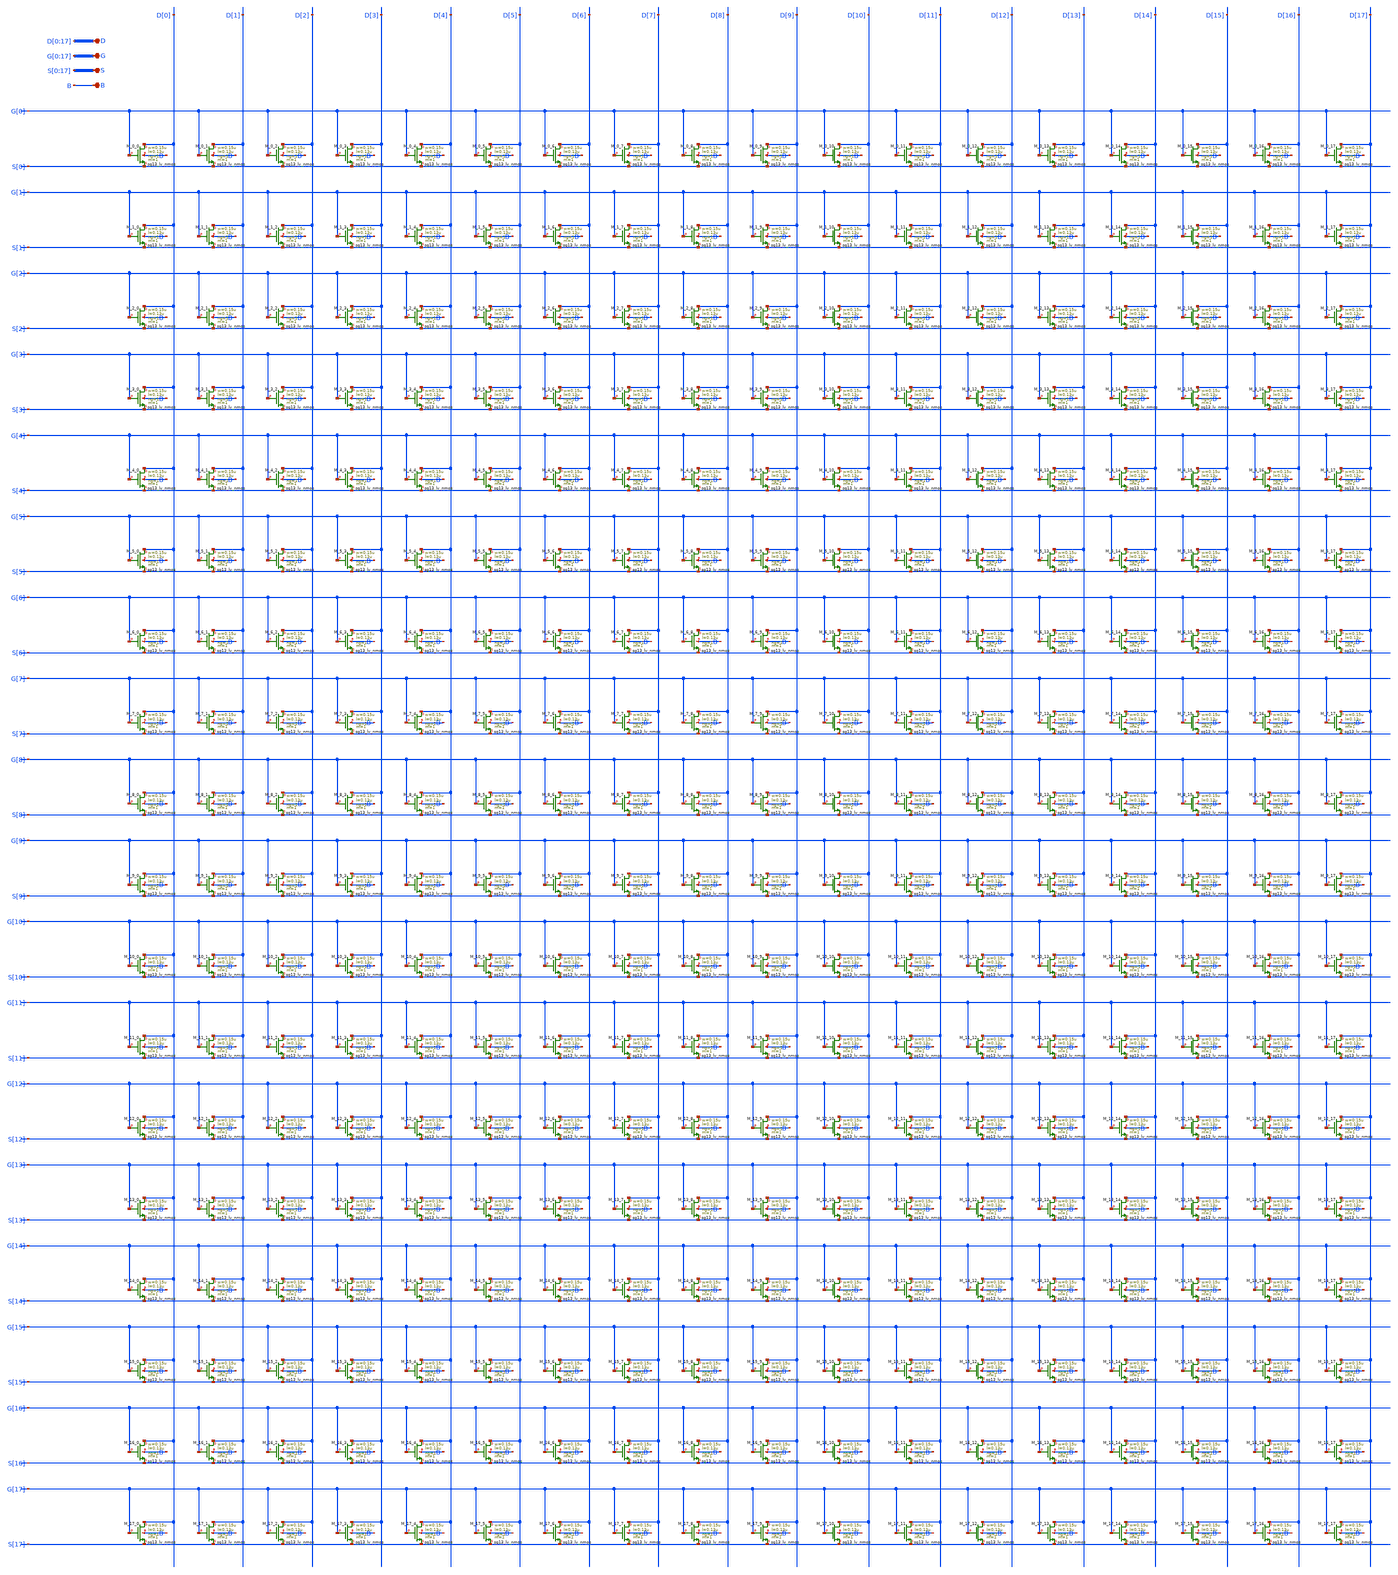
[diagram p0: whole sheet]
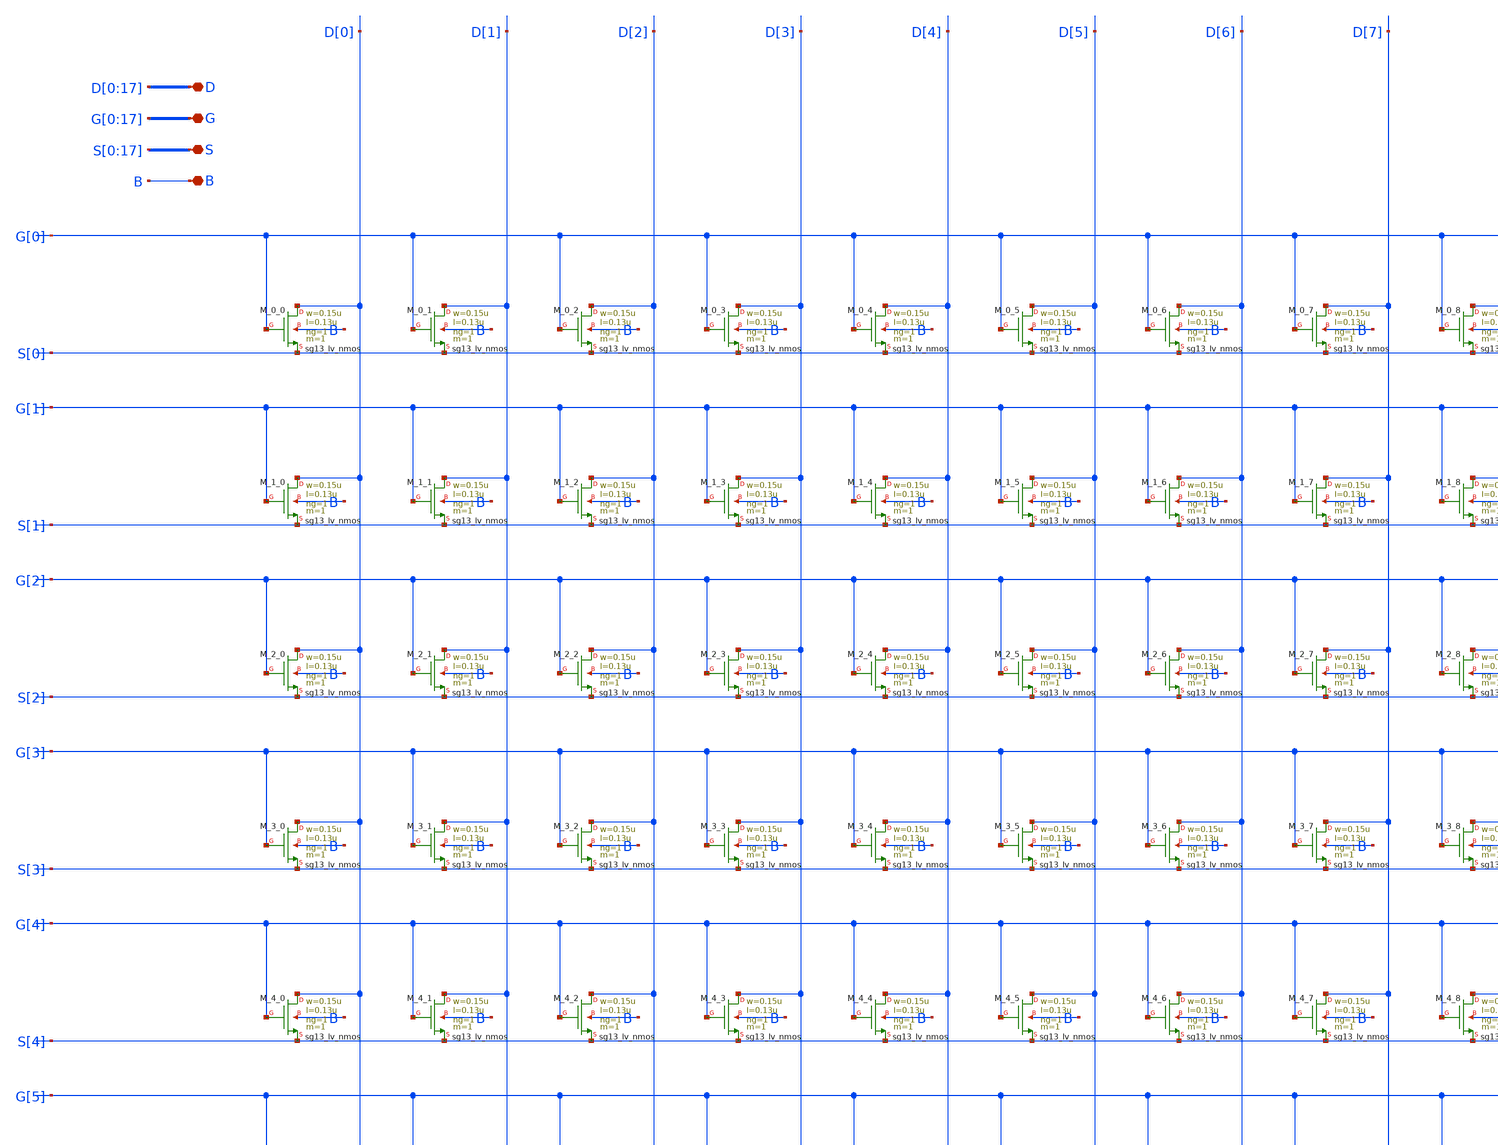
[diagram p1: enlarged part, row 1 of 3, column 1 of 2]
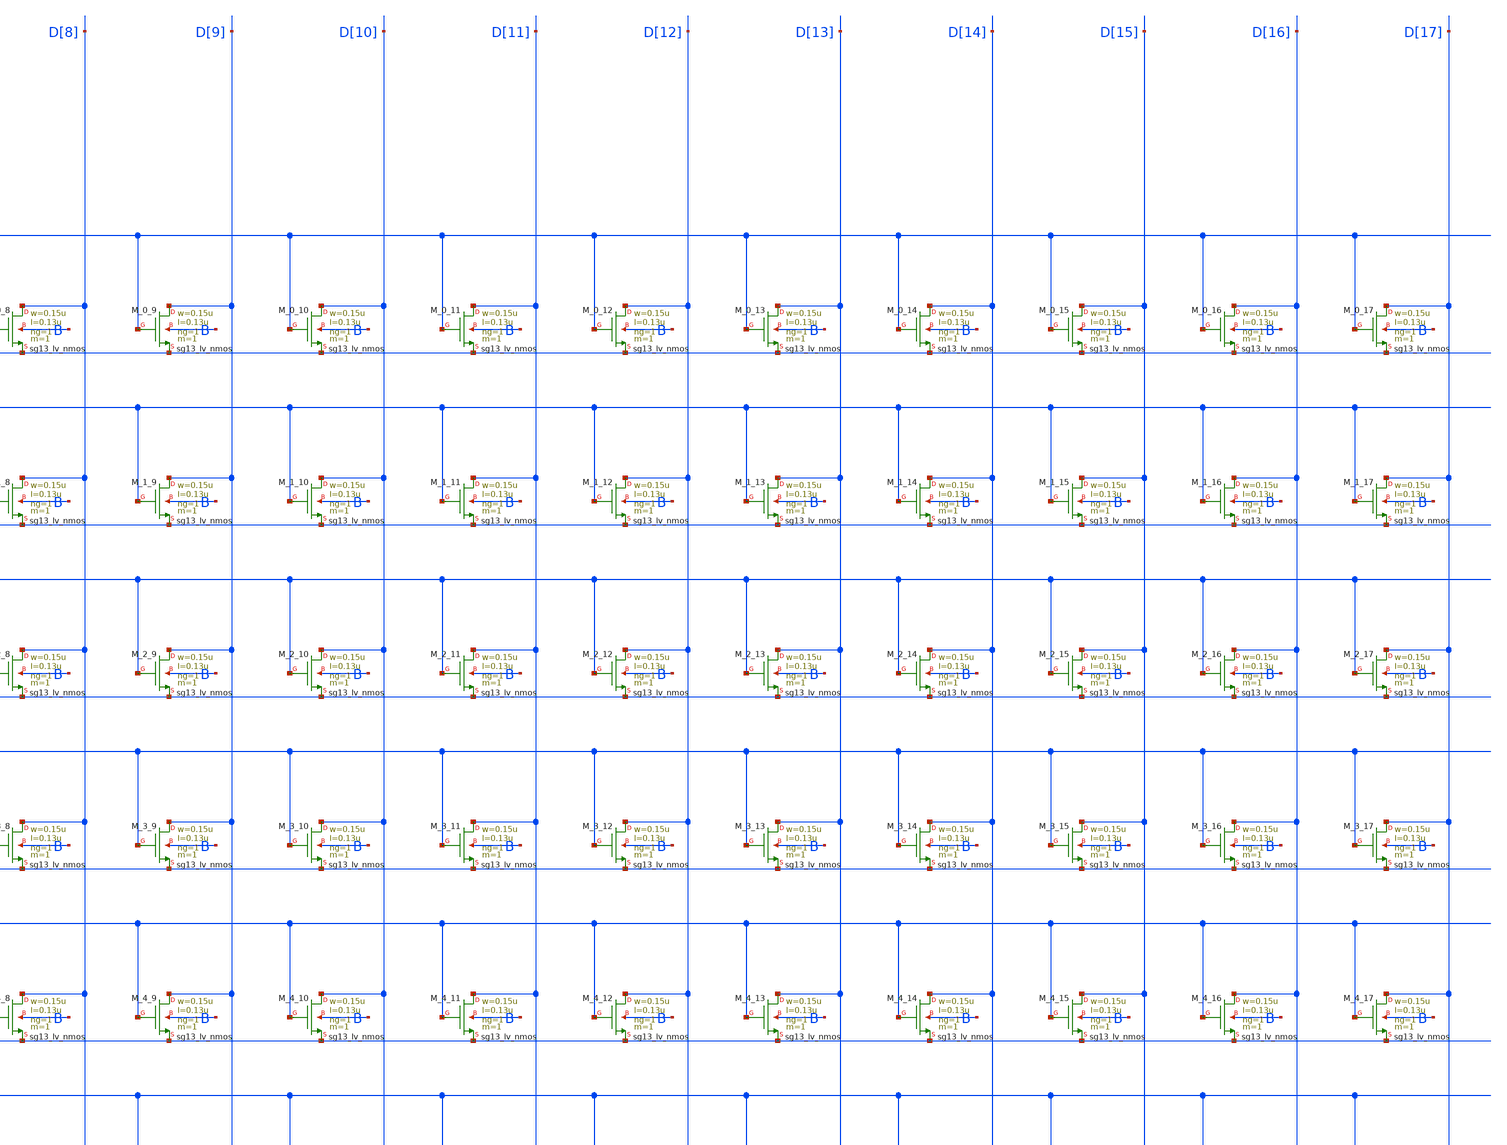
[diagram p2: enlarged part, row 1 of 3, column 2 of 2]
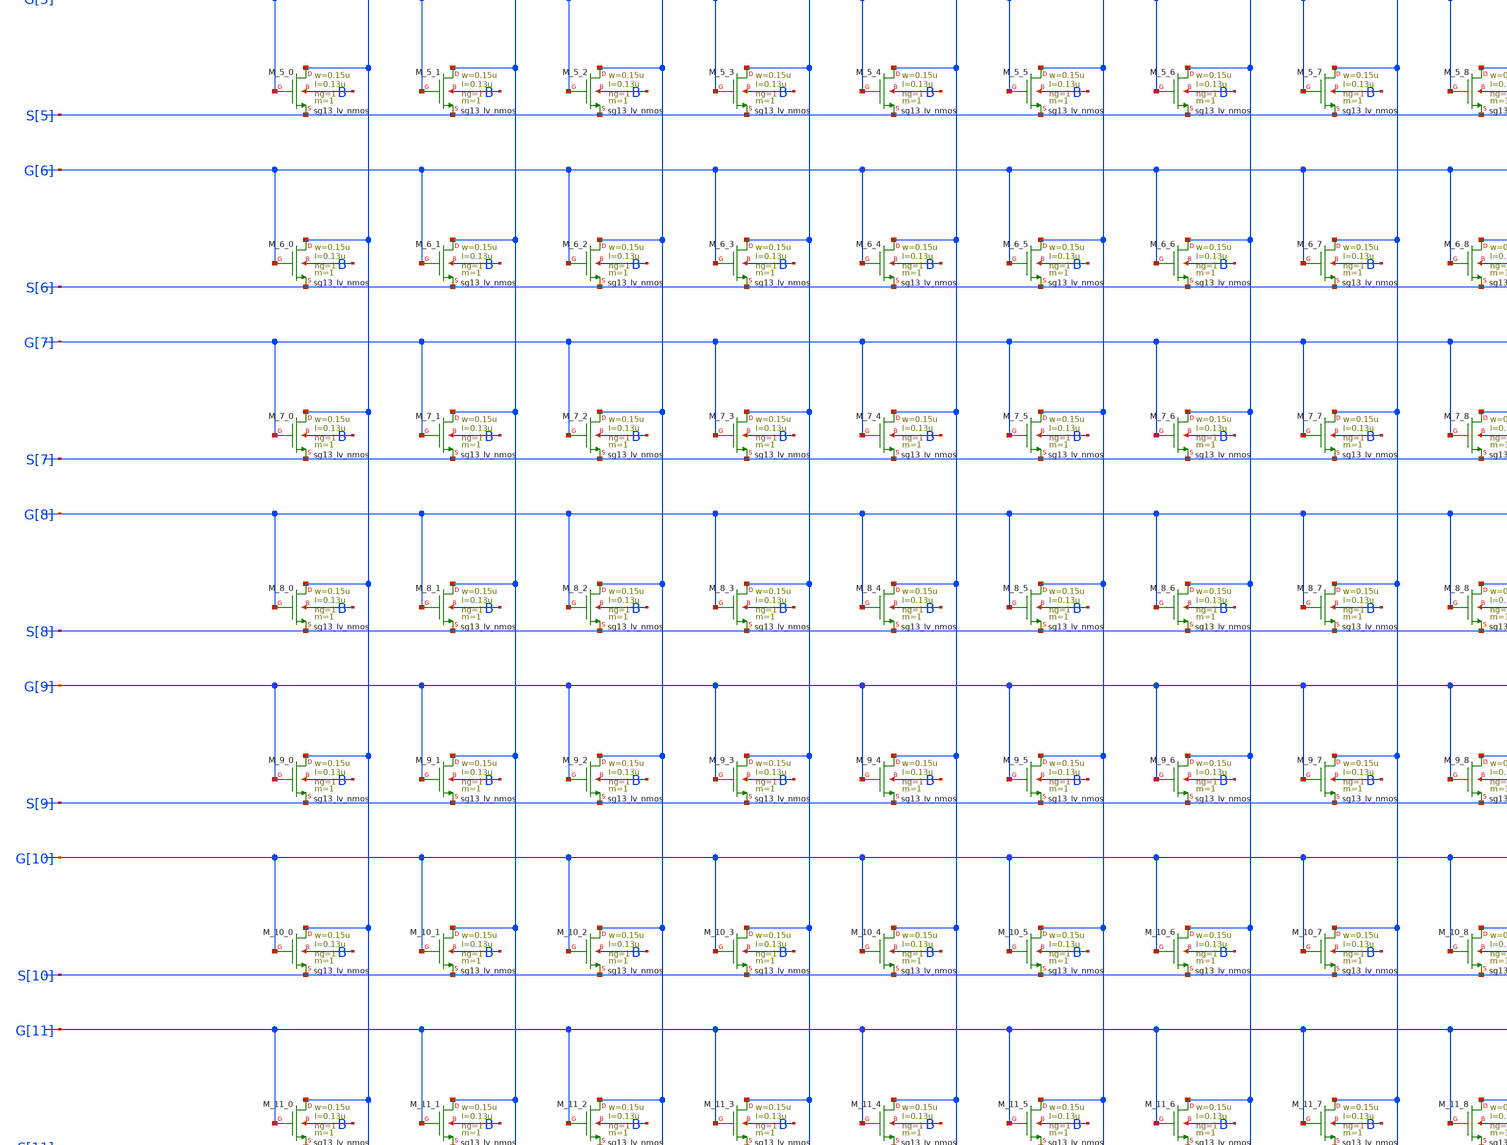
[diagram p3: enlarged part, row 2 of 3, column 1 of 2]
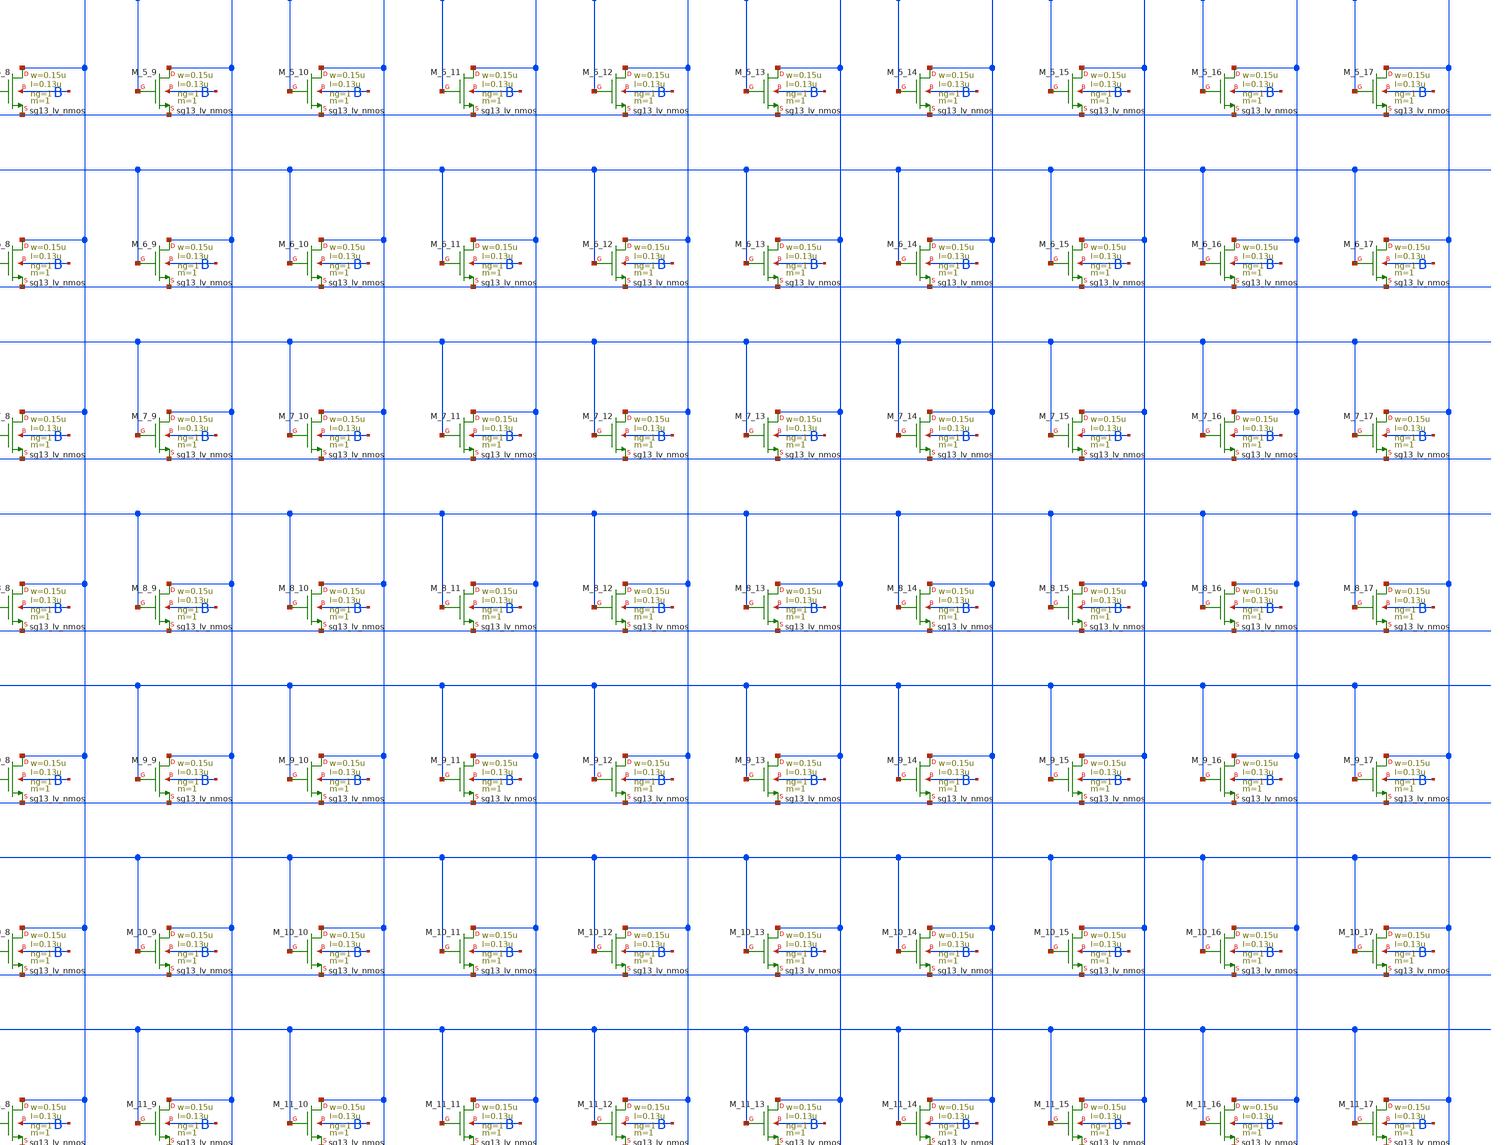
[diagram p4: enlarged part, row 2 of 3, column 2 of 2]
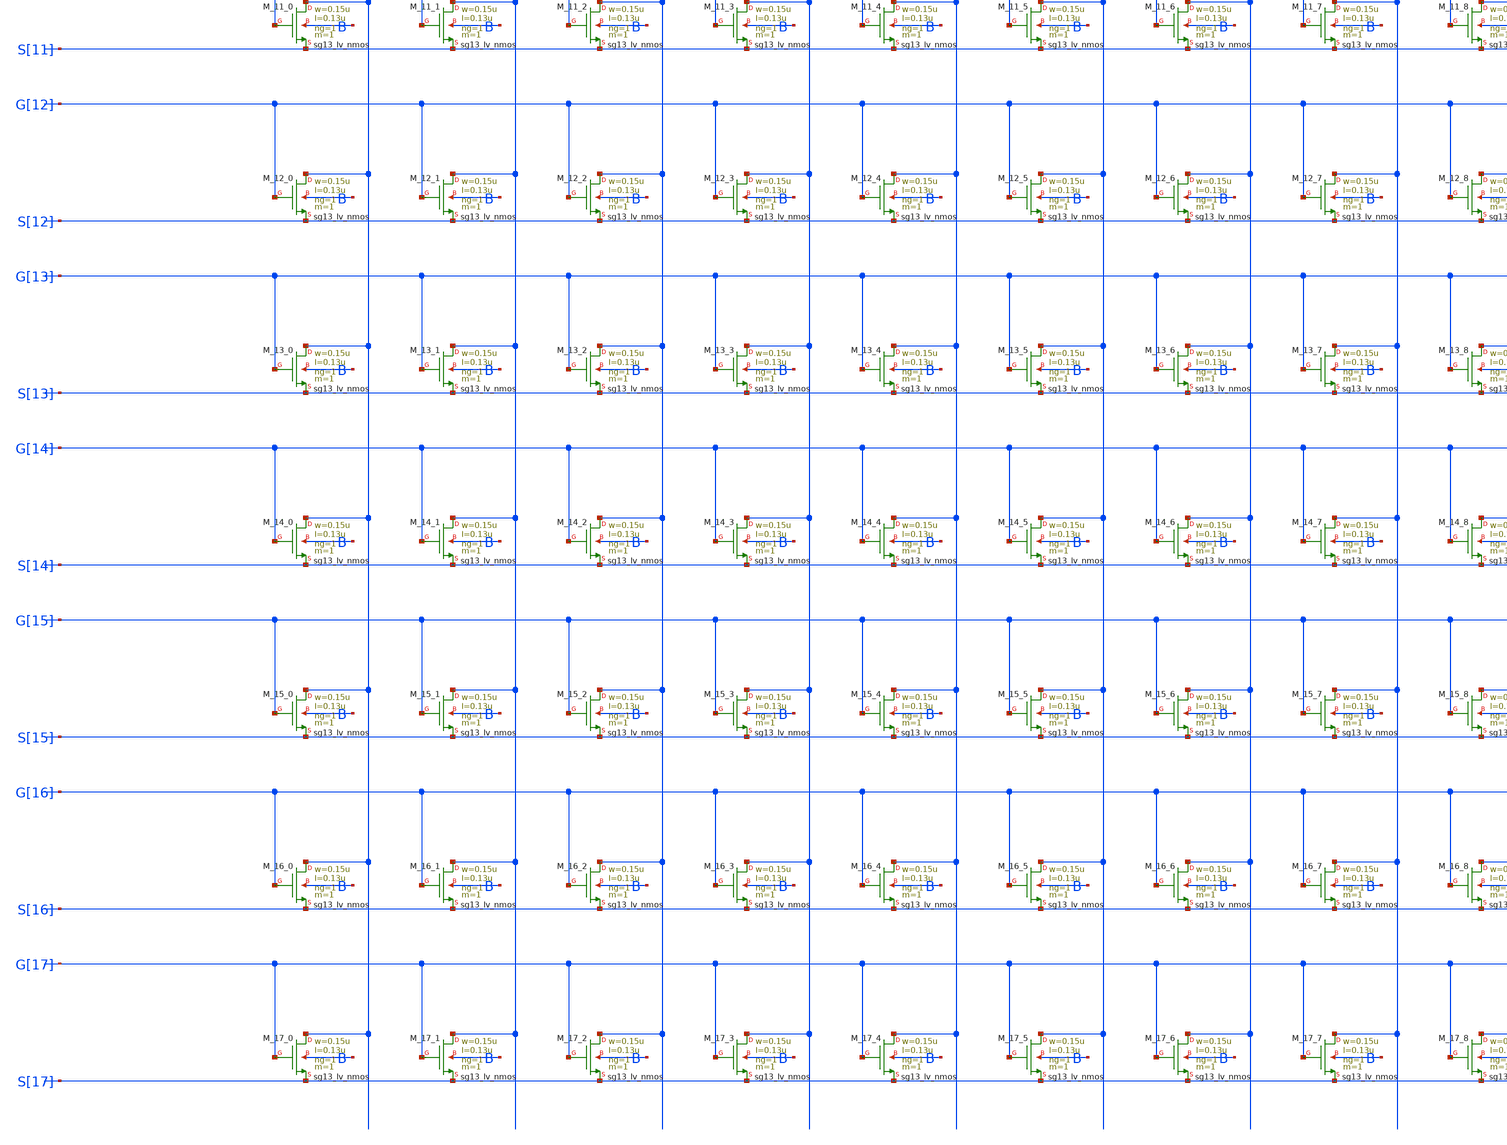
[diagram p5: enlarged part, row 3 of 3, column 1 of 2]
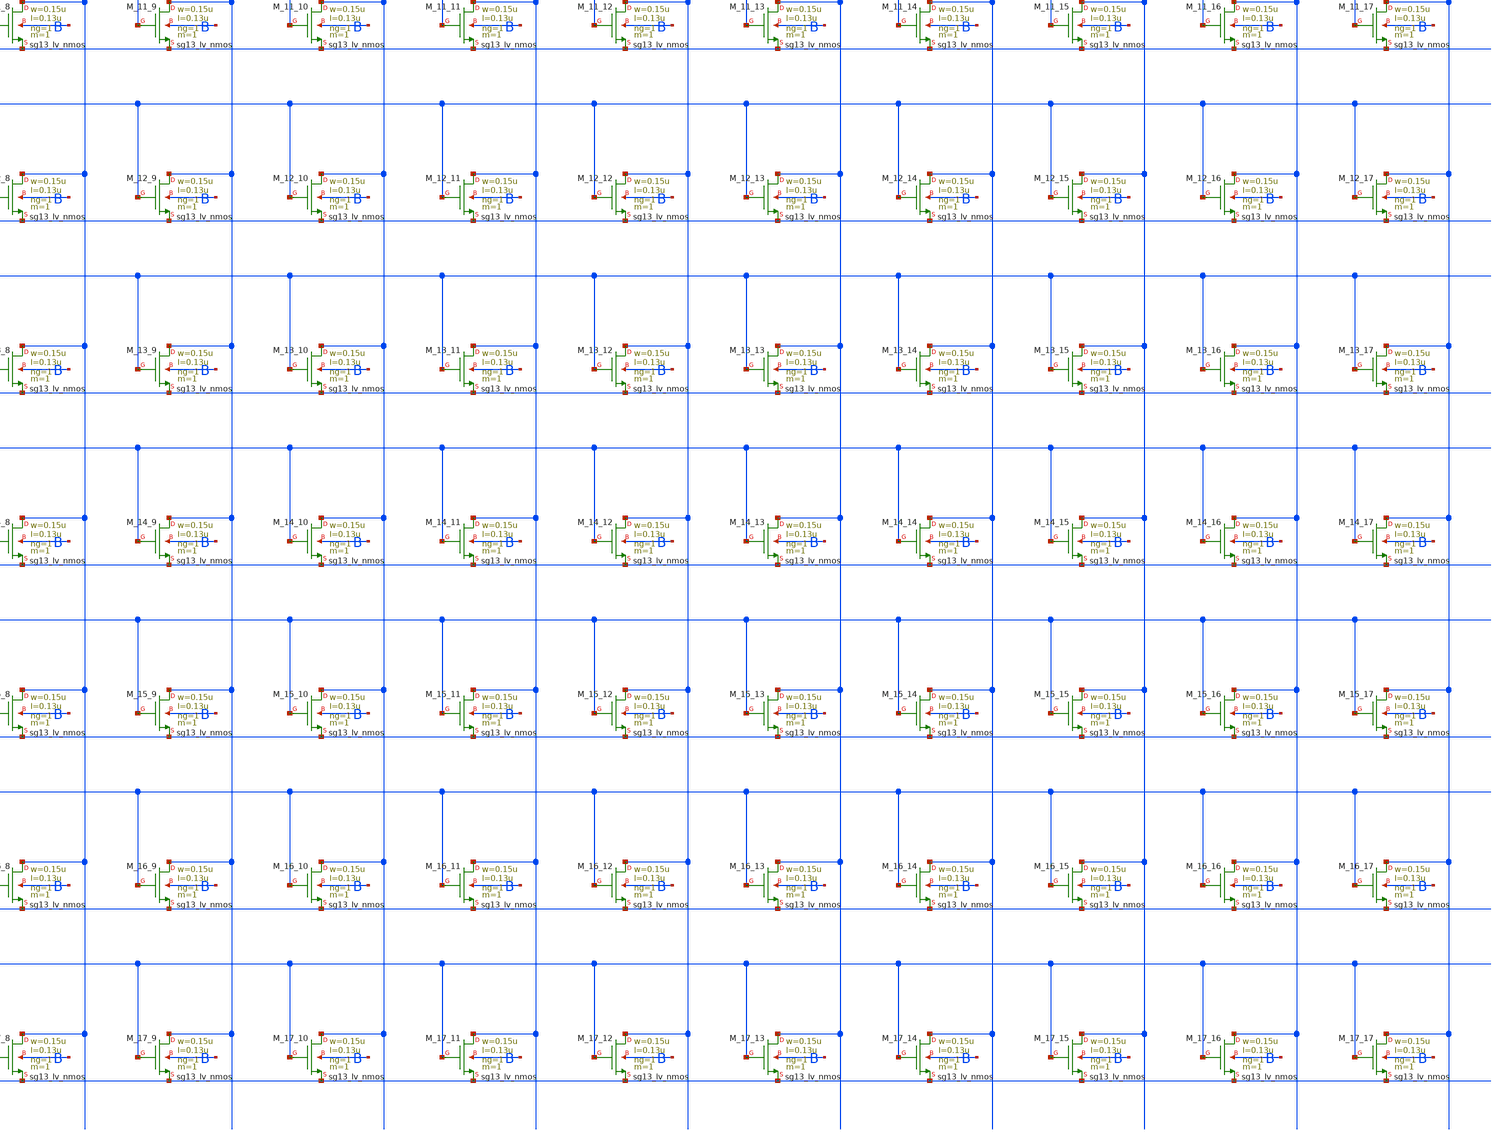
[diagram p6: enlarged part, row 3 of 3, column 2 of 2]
** sch_path: design_data/xschem/new_DUT/18x18/W0p15u_L0p13u.sch
**.subckt W0p15u_L0p13u D G S B
*.iopin D
*.iopin G
*.iopin S
*.iopin B
XM_0_0 D[0] G[0] S[0] B sg13_lv_nmos w=0.15u l=0.13u ng=1 m=1 mm_ok=1
XM_0_1 D[1] G[0] S[0] B sg13_lv_nmos w=0.15u l=0.13u ng=1 m=1 mm_ok=1
XM_0_2 D[2] G[0] S[0] B sg13_lv_nmos w=0.15u l=0.13u ng=1 m=1 mm_ok=1
XM_0_3 D[3] G[0] S[0] B sg13_lv_nmos w=0.15u l=0.13u ng=1 m=1 mm_ok=1
XM_0_4 D[4] G[0] S[0] B sg13_lv_nmos w=0.15u l=0.13u ng=1 m=1 mm_ok=1
XM_0_5 D[5] G[0] S[0] B sg13_lv_nmos w=0.15u l=0.13u ng=1 m=1 mm_ok=1
XM_0_6 D[6] G[0] S[0] B sg13_lv_nmos w=0.15u l=0.13u ng=1 m=1 mm_ok=1
XM_0_7 D[7] G[0] S[0] B sg13_lv_nmos w=0.15u l=0.13u ng=1 m=1 mm_ok=1
XM_0_8 D[8] G[0] S[0] B sg13_lv_nmos w=0.15u l=0.13u ng=1 m=1 mm_ok=1
XM_0_9 D[9] G[0] S[0] B sg13_lv_nmos w=0.15u l=0.13u ng=1 m=1 mm_ok=1
XM_0_10 D[10] G[0] S[0] B sg13_lv_nmos w=0.15u l=0.13u ng=1 m=1 mm_ok=1
XM_0_11 D[11] G[0] S[0] B sg13_lv_nmos w=0.15u l=0.13u ng=1 m=1 mm_ok=1
XM_0_12 D[12] G[0] S[0] B sg13_lv_nmos w=0.15u l=0.13u ng=1 m=1 mm_ok=1
XM_0_13 D[13] G[0] S[0] B sg13_lv_nmos w=0.15u l=0.13u ng=1 m=1 mm_ok=1
XM_0_14 D[14] G[0] S[0] B sg13_lv_nmos w=0.15u l=0.13u ng=1 m=1 mm_ok=1
XM_0_15 D[15] G[0] S[0] B sg13_lv_nmos w=0.15u l=0.13u ng=1 m=1 mm_ok=1
XM_0_16 D[16] G[0] S[0] B sg13_lv_nmos w=0.15u l=0.13u ng=1 m=1 mm_ok=1
XM_0_17 D[17] G[0] S[0] B sg13_lv_nmos w=0.15u l=0.13u ng=1 m=1 mm_ok=1
XM_1_0 D[0] G[1] S[1] B sg13_lv_nmos w=0.15u l=0.13u ng=1 m=1 mm_ok=1
XM_1_1 D[1] G[1] S[1] B sg13_lv_nmos w=0.15u l=0.13u ng=1 m=1 mm_ok=1
XM_1_2 D[2] G[1] S[1] B sg13_lv_nmos w=0.15u l=0.13u ng=1 m=1 mm_ok=1
XM_1_3 D[3] G[1] S[1] B sg13_lv_nmos w=0.15u l=0.13u ng=1 m=1 mm_ok=1
XM_1_4 D[4] G[1] S[1] B sg13_lv_nmos w=0.15u l=0.13u ng=1 m=1 mm_ok=1
XM_1_5 D[5] G[1] S[1] B sg13_lv_nmos w=0.15u l=0.13u ng=1 m=1 mm_ok=1
XM_1_6 D[6] G[1] S[1] B sg13_lv_nmos w=0.15u l=0.13u ng=1 m=1 mm_ok=1
XM_1_7 D[7] G[1] S[1] B sg13_lv_nmos w=0.15u l=0.13u ng=1 m=1 mm_ok=1
XM_1_8 D[8] G[1] S[1] B sg13_lv_nmos w=0.15u l=0.13u ng=1 m=1 mm_ok=1
XM_1_9 D[9] G[1] S[1] B sg13_lv_nmos w=0.15u l=0.13u ng=1 m=1 mm_ok=1
XM_1_10 D[10] G[1] S[1] B sg13_lv_nmos w=0.15u l=0.13u ng=1 m=1 mm_ok=1
XM_1_11 D[11] G[1] S[1] B sg13_lv_nmos w=0.15u l=0.13u ng=1 m=1 mm_ok=1
XM_1_12 D[12] G[1] S[1] B sg13_lv_nmos w=0.15u l=0.13u ng=1 m=1 mm_ok=1
XM_1_13 D[13] G[1] S[1] B sg13_lv_nmos w=0.15u l=0.13u ng=1 m=1 mm_ok=1
XM_1_14 D[14] G[1] S[1] B sg13_lv_nmos w=0.15u l=0.13u ng=1 m=1 mm_ok=1
XM_1_15 D[15] G[1] S[1] B sg13_lv_nmos w=0.15u l=0.13u ng=1 m=1 mm_ok=1
XM_1_16 D[16] G[1] S[1] B sg13_lv_nmos w=0.15u l=0.13u ng=1 m=1 mm_ok=1
XM_1_17 D[17] G[1] S[1] B sg13_lv_nmos w=0.15u l=0.13u ng=1 m=1 mm_ok=1
XM_2_0 D[0] G[2] S[2] B sg13_lv_nmos w=0.15u l=0.13u ng=1 m=1 mm_ok=1
XM_2_1 D[1] G[2] S[2] B sg13_lv_nmos w=0.15u l=0.13u ng=1 m=1 mm_ok=1
XM_2_2 D[2] G[2] S[2] B sg13_lv_nmos w=0.15u l=0.13u ng=1 m=1 mm_ok=1
XM_2_3 D[3] G[2] S[2] B sg13_lv_nmos w=0.15u l=0.13u ng=1 m=1 mm_ok=1
XM_2_4 D[4] G[2] S[2] B sg13_lv_nmos w=0.15u l=0.13u ng=1 m=1 mm_ok=1
XM_2_5 D[5] G[2] S[2] B sg13_lv_nmos w=0.15u l=0.13u ng=1 m=1 mm_ok=1
XM_2_6 D[6] G[2] S[2] B sg13_lv_nmos w=0.15u l=0.13u ng=1 m=1 mm_ok=1
XM_2_7 D[7] G[2] S[2] B sg13_lv_nmos w=0.15u l=0.13u ng=1 m=1 mm_ok=1
XM_2_8 D[8] G[2] S[2] B sg13_lv_nmos w=0.15u l=0.13u ng=1 m=1 mm_ok=1
XM_2_9 D[9] G[2] S[2] B sg13_lv_nmos w=0.15u l=0.13u ng=1 m=1 mm_ok=1
XM_2_10 D[10] G[2] S[2] B sg13_lv_nmos w=0.15u l=0.13u ng=1 m=1 mm_ok=1
XM_2_11 D[11] G[2] S[2] B sg13_lv_nmos w=0.15u l=0.13u ng=1 m=1 mm_ok=1
XM_2_12 D[12] G[2] S[2] B sg13_lv_nmos w=0.15u l=0.13u ng=1 m=1 mm_ok=1
XM_2_13 D[13] G[2] S[2] B sg13_lv_nmos w=0.15u l=0.13u ng=1 m=1 mm_ok=1
XM_2_14 D[14] G[2] S[2] B sg13_lv_nmos w=0.15u l=0.13u ng=1 m=1 mm_ok=1
XM_2_15 D[15] G[2] S[2] B sg13_lv_nmos w=0.15u l=0.13u ng=1 m=1 mm_ok=1
XM_2_16 D[16] G[2] S[2] B sg13_lv_nmos w=0.15u l=0.13u ng=1 m=1 mm_ok=1
XM_2_17 D[17] G[2] S[2] B sg13_lv_nmos w=0.15u l=0.13u ng=1 m=1 mm_ok=1
XM_3_0 D[0] G[3] S[3] B sg13_lv_nmos w=0.15u l=0.13u ng=1 m=1 mm_ok=1
XM_3_1 D[1] G[3] S[3] B sg13_lv_nmos w=0.15u l=0.13u ng=1 m=1 mm_ok=1
XM_3_2 D[2] G[3] S[3] B sg13_lv_nmos w=0.15u l=0.13u ng=1 m=1 mm_ok=1
XM_3_3 D[3] G[3] S[3] B sg13_lv_nmos w=0.15u l=0.13u ng=1 m=1 mm_ok=1
XM_3_4 D[4] G[3] S[3] B sg13_lv_nmos w=0.15u l=0.13u ng=1 m=1 mm_ok=1
XM_3_5 D[5] G[3] S[3] B sg13_lv_nmos w=0.15u l=0.13u ng=1 m=1 mm_ok=1
XM_3_6 D[6] G[3] S[3] B sg13_lv_nmos w=0.15u l=0.13u ng=1 m=1 mm_ok=1
XM_3_7 D[7] G[3] S[3] B sg13_lv_nmos w=0.15u l=0.13u ng=1 m=1 mm_ok=1
XM_3_8 D[8] G[3] S[3] B sg13_lv_nmos w=0.15u l=0.13u ng=1 m=1 mm_ok=1
XM_3_9 D[9] G[3] S[3] B sg13_lv_nmos w=0.15u l=0.13u ng=1 m=1 mm_ok=1
XM_3_10 D[10] G[3] S[3] B sg13_lv_nmos w=0.15u l=0.13u ng=1 m=1 mm_ok=1
XM_3_11 D[11] G[3] S[3] B sg13_lv_nmos w=0.15u l=0.13u ng=1 m=1 mm_ok=1
XM_3_12 D[12] G[3] S[3] B sg13_lv_nmos w=0.15u l=0.13u ng=1 m=1 mm_ok=1
XM_3_13 D[13] G[3] S[3] B sg13_lv_nmos w=0.15u l=0.13u ng=1 m=1 mm_ok=1
XM_3_14 D[14] G[3] S[3] B sg13_lv_nmos w=0.15u l=0.13u ng=1 m=1 mm_ok=1
XM_3_15 D[15] G[3] S[3] B sg13_lv_nmos w=0.15u l=0.13u ng=1 m=1 mm_ok=1
XM_3_16 D[16] G[3] S[3] B sg13_lv_nmos w=0.15u l=0.13u ng=1 m=1 mm_ok=1
XM_3_17 D[17] G[3] S[3] B sg13_lv_nmos w=0.15u l=0.13u ng=1 m=1 mm_ok=1
XM_4_0 D[0] G[4] S[4] B sg13_lv_nmos w=0.15u l=0.13u ng=1 m=1 mm_ok=1
XM_4_1 D[1] G[4] S[4] B sg13_lv_nmos w=0.15u l=0.13u ng=1 m=1 mm_ok=1
XM_4_2 D[2] G[4] S[4] B sg13_lv_nmos w=0.15u l=0.13u ng=1 m=1 mm_ok=1
XM_4_3 D[3] G[4] S[4] B sg13_lv_nmos w=0.15u l=0.13u ng=1 m=1 mm_ok=1
XM_4_4 D[4] G[4] S[4] B sg13_lv_nmos w=0.15u l=0.13u ng=1 m=1 mm_ok=1
XM_4_5 D[5] G[4] S[4] B sg13_lv_nmos w=0.15u l=0.13u ng=1 m=1 mm_ok=1
XM_4_6 D[6] G[4] S[4] B sg13_lv_nmos w=0.15u l=0.13u ng=1 m=1 mm_ok=1
XM_4_7 D[7] G[4] S[4] B sg13_lv_nmos w=0.15u l=0.13u ng=1 m=1 mm_ok=1
XM_4_8 D[8] G[4] S[4] B sg13_lv_nmos w=0.15u l=0.13u ng=1 m=1 mm_ok=1
XM_4_9 D[9] G[4] S[4] B sg13_lv_nmos w=0.15u l=0.13u ng=1 m=1 mm_ok=1
XM_4_10 D[10] G[4] S[4] B sg13_lv_nmos w=0.15u l=0.13u ng=1 m=1 mm_ok=1
XM_4_11 D[11] G[4] S[4] B sg13_lv_nmos w=0.15u l=0.13u ng=1 m=1 mm_ok=1
XM_4_12 D[12] G[4] S[4] B sg13_lv_nmos w=0.15u l=0.13u ng=1 m=1 mm_ok=1
XM_4_13 D[13] G[4] S[4] B sg13_lv_nmos w=0.15u l=0.13u ng=1 m=1 mm_ok=1
XM_4_14 D[14] G[4] S[4] B sg13_lv_nmos w=0.15u l=0.13u ng=1 m=1 mm_ok=1
XM_4_15 D[15] G[4] S[4] B sg13_lv_nmos w=0.15u l=0.13u ng=1 m=1 mm_ok=1
XM_4_16 D[16] G[4] S[4] B sg13_lv_nmos w=0.15u l=0.13u ng=1 m=1 mm_ok=1
XM_4_17 D[17] G[4] S[4] B sg13_lv_nmos w=0.15u l=0.13u ng=1 m=1 mm_ok=1
XM_5_0 D[0] G[5] S[5] B sg13_lv_nmos w=0.15u l=0.13u ng=1 m=1 mm_ok=1
XM_5_1 D[1] G[5] S[5] B sg13_lv_nmos w=0.15u l=0.13u ng=1 m=1 mm_ok=1
XM_5_2 D[2] G[5] S[5] B sg13_lv_nmos w=0.15u l=0.13u ng=1 m=1 mm_ok=1
XM_5_3 D[3] G[5] S[5] B sg13_lv_nmos w=0.15u l=0.13u ng=1 m=1 mm_ok=1
XM_5_4 D[4] G[5] S[5] B sg13_lv_nmos w=0.15u l=0.13u ng=1 m=1 mm_ok=1
XM_5_5 D[5] G[5] S[5] B sg13_lv_nmos w=0.15u l=0.13u ng=1 m=1 mm_ok=1
XM_5_6 D[6] G[5] S[5] B sg13_lv_nmos w=0.15u l=0.13u ng=1 m=1 mm_ok=1
XM_5_7 D[7] G[5] S[5] B sg13_lv_nmos w=0.15u l=0.13u ng=1 m=1 mm_ok=1
XM_5_8 D[8] G[5] S[5] B sg13_lv_nmos w=0.15u l=0.13u ng=1 m=1 mm_ok=1
XM_5_9 D[9] G[5] S[5] B sg13_lv_nmos w=0.15u l=0.13u ng=1 m=1 mm_ok=1
XM_5_10 D[10] G[5] S[5] B sg13_lv_nmos w=0.15u l=0.13u ng=1 m=1 mm_ok=1
XM_5_11 D[11] G[5] S[5] B sg13_lv_nmos w=0.15u l=0.13u ng=1 m=1 mm_ok=1
XM_5_12 D[12] G[5] S[5] B sg13_lv_nmos w=0.15u l=0.13u ng=1 m=1 mm_ok=1
XM_5_13 D[13] G[5] S[5] B sg13_lv_nmos w=0.15u l=0.13u ng=1 m=1 mm_ok=1
XM_5_14 D[14] G[5] S[5] B sg13_lv_nmos w=0.15u l=0.13u ng=1 m=1 mm_ok=1
XM_5_15 D[15] G[5] S[5] B sg13_lv_nmos w=0.15u l=0.13u ng=1 m=1 mm_ok=1
XM_5_16 D[16] G[5] S[5] B sg13_lv_nmos w=0.15u l=0.13u ng=1 m=1 mm_ok=1
XM_5_17 D[17] G[5] S[5] B sg13_lv_nmos w=0.15u l=0.13u ng=1 m=1 mm_ok=1
XM_6_0 D[0] G[6] S[6] B sg13_lv_nmos w=0.15u l=0.13u ng=1 m=1 mm_ok=1
XM_6_1 D[1] G[6] S[6] B sg13_lv_nmos w=0.15u l=0.13u ng=1 m=1 mm_ok=1
XM_6_2 D[2] G[6] S[6] B sg13_lv_nmos w=0.15u l=0.13u ng=1 m=1 mm_ok=1
XM_6_3 D[3] G[6] S[6] B sg13_lv_nmos w=0.15u l=0.13u ng=1 m=1 mm_ok=1
XM_6_4 D[4] G[6] S[6] B sg13_lv_nmos w=0.15u l=0.13u ng=1 m=1 mm_ok=1
XM_6_5 D[5] G[6] S[6] B sg13_lv_nmos w=0.15u l=0.13u ng=1 m=1 mm_ok=1
XM_6_6 D[6] G[6] S[6] B sg13_lv_nmos w=0.15u l=0.13u ng=1 m=1 mm_ok=1
XM_6_7 D[7] G[6] S[6] B sg13_lv_nmos w=0.15u l=0.13u ng=1 m=1 mm_ok=1
XM_6_8 D[8] G[6] S[6] B sg13_lv_nmos w=0.15u l=0.13u ng=1 m=1 mm_ok=1
XM_6_9 D[9] G[6] S[6] B sg13_lv_nmos w=0.15u l=0.13u ng=1 m=1 mm_ok=1
XM_6_10 D[10] G[6] S[6] B sg13_lv_nmos w=0.15u l=0.13u ng=1 m=1 mm_ok=1
XM_6_11 D[11] G[6] S[6] B sg13_lv_nmos w=0.15u l=0.13u ng=1 m=1 mm_ok=1
XM_6_12 D[12] G[6] S[6] B sg13_lv_nmos w=0.15u l=0.13u ng=1 m=1 mm_ok=1
XM_6_13 D[13] G[6] S[6] B sg13_lv_nmos w=0.15u l=0.13u ng=1 m=1 mm_ok=1
XM_6_14 D[14] G[6] S[6] B sg13_lv_nmos w=0.15u l=0.13u ng=1 m=1 mm_ok=1
XM_6_15 D[15] G[6] S[6] B sg13_lv_nmos w=0.15u l=0.13u ng=1 m=1 mm_ok=1
XM_6_16 D[16] G[6] S[6] B sg13_lv_nmos w=0.15u l=0.13u ng=1 m=1 mm_ok=1
XM_6_17 D[17] G[6] S[6] B sg13_lv_nmos w=0.15u l=0.13u ng=1 m=1 mm_ok=1
XM_7_0 D[0] G[7] S[7] B sg13_lv_nmos w=0.15u l=0.13u ng=1 m=1 mm_ok=1
XM_7_1 D[1] G[7] S[7] B sg13_lv_nmos w=0.15u l=0.13u ng=1 m=1 mm_ok=1
XM_7_2 D[2] G[7] S[7] B sg13_lv_nmos w=0.15u l=0.13u ng=1 m=1 mm_ok=1
XM_7_3 D[3] G[7] S[7] B sg13_lv_nmos w=0.15u l=0.13u ng=1 m=1 mm_ok=1
XM_7_4 D[4] G[7] S[7] B sg13_lv_nmos w=0.15u l=0.13u ng=1 m=1 mm_ok=1
XM_7_5 D[5] G[7] S[7] B sg13_lv_nmos w=0.15u l=0.13u ng=1 m=1 mm_ok=1
XM_7_6 D[6] G[7] S[7] B sg13_lv_nmos w=0.15u l=0.13u ng=1 m=1 mm_ok=1
XM_7_7 D[7] G[7] S[7] B sg13_lv_nmos w=0.15u l=0.13u ng=1 m=1 mm_ok=1
XM_7_8 D[8] G[7] S[7] B sg13_lv_nmos w=0.15u l=0.13u ng=1 m=1 mm_ok=1
XM_7_9 D[9] G[7] S[7] B sg13_lv_nmos w=0.15u l=0.13u ng=1 m=1 mm_ok=1
XM_7_10 D[10] G[7] S[7] B sg13_lv_nmos w=0.15u l=0.13u ng=1 m=1 mm_ok=1
XM_7_11 D[11] G[7] S[7] B sg13_lv_nmos w=0.15u l=0.13u ng=1 m=1 mm_ok=1
XM_7_12 D[12] G[7] S[7] B sg13_lv_nmos w=0.15u l=0.13u ng=1 m=1 mm_ok=1
XM_7_13 D[13] G[7] S[7] B sg13_lv_nmos w=0.15u l=0.13u ng=1 m=1 mm_ok=1
XM_7_14 D[14] G[7] S[7] B sg13_lv_nmos w=0.15u l=0.13u ng=1 m=1 mm_ok=1
XM_7_15 D[15] G[7] S[7] B sg13_lv_nmos w=0.15u l=0.13u ng=1 m=1 mm_ok=1
XM_7_16 D[16] G[7] S[7] B sg13_lv_nmos w=0.15u l=0.13u ng=1 m=1 mm_ok=1
XM_7_17 D[17] G[7] S[7] B sg13_lv_nmos w=0.15u l=0.13u ng=1 m=1 mm_ok=1
XM_8_0 D[0] G[8] S[8] B sg13_lv_nmos w=0.15u l=0.13u ng=1 m=1 mm_ok=1
XM_8_1 D[1] G[8] S[8] B sg13_lv_nmos w=0.15u l=0.13u ng=1 m=1 mm_ok=1
XM_8_2 D[2] G[8] S[8] B sg13_lv_nmos w=0.15u l=0.13u ng=1 m=1 mm_ok=1
XM_8_3 D[3] G[8] S[8] B sg13_lv_nmos w=0.15u l=0.13u ng=1 m=1 mm_ok=1
XM_8_4 D[4] G[8] S[8] B sg13_lv_nmos w=0.15u l=0.13u ng=1 m=1 mm_ok=1
XM_8_5 D[5] G[8] S[8] B sg13_lv_nmos w=0.15u l=0.13u ng=1 m=1 mm_ok=1
XM_8_6 D[6] G[8] S[8] B sg13_lv_nmos w=0.15u l=0.13u ng=1 m=1 mm_ok=1
XM_8_7 D[7] G[8] S[8] B sg13_lv_nmos w=0.15u l=0.13u ng=1 m=1 mm_ok=1
XM_8_8 D[8] G[8] S[8] B sg13_lv_nmos w=0.15u l=0.13u ng=1 m=1 mm_ok=1
XM_8_9 D[9] G[8] S[8] B sg13_lv_nmos w=0.15u l=0.13u ng=1 m=1 mm_ok=1
XM_8_10 D[10] G[8] S[8] B sg13_lv_nmos w=0.15u l=0.13u ng=1 m=1 mm_ok=1
XM_8_11 D[11] G[8] S[8] B sg13_lv_nmos w=0.15u l=0.13u ng=1 m=1 mm_ok=1
XM_8_12 D[12] G[8] S[8] B sg13_lv_nmos w=0.15u l=0.13u ng=1 m=1 mm_ok=1
XM_8_13 D[13] G[8] S[8] B sg13_lv_nmos w=0.15u l=0.13u ng=1 m=1 mm_ok=1
XM_8_14 D[14] G[8] S[8] B sg13_lv_nmos w=0.15u l=0.13u ng=1 m=1 mm_ok=1
XM_8_15 D[15] G[8] S[8] B sg13_lv_nmos w=0.15u l=0.13u ng=1 m=1 mm_ok=1
XM_8_16 D[16] G[8] S[8] B sg13_lv_nmos w=0.15u l=0.13u ng=1 m=1 mm_ok=1
XM_8_17 D[17] G[8] S[8] B sg13_lv_nmos w=0.15u l=0.13u ng=1 m=1 mm_ok=1
XM_9_0 D[0] G[9] S[9] B sg13_lv_nmos w=0.15u l=0.13u ng=1 m=1 mm_ok=1
XM_9_1 D[1] G[9] S[9] B sg13_lv_nmos w=0.15u l=0.13u ng=1 m=1 mm_ok=1
XM_9_2 D[2] G[9] S[9] B sg13_lv_nmos w=0.15u l=0.13u ng=1 m=1 mm_ok=1
XM_9_3 D[3] G[9] S[9] B sg13_lv_nmos w=0.15u l=0.13u ng=1 m=1 mm_ok=1
XM_9_4 D[4] G[9] S[9] B sg13_lv_nmos w=0.15u l=0.13u ng=1 m=1 mm_ok=1
XM_9_5 D[5] G[9] S[9] B sg13_lv_nmos w=0.15u l=0.13u ng=1 m=1 mm_ok=1
XM_9_6 D[6] G[9] S[9] B sg13_lv_nmos w=0.15u l=0.13u ng=1 m=1 mm_ok=1
XM_9_7 D[7] G[9] S[9] B sg13_lv_nmos w=0.15u l=0.13u ng=1 m=1 mm_ok=1
XM_9_8 D[8] G[9] S[9] B sg13_lv_nmos w=0.15u l=0.13u ng=1 m=1 mm_ok=1
XM_9_9 D[9] G[9] S[9] B sg13_lv_nmos w=0.15u l=0.13u ng=1 m=1 mm_ok=1
XM_9_10 D[10] G[9] S[9] B sg13_lv_nmos w=0.15u l=0.13u ng=1 m=1 mm_ok=1
XM_9_11 D[11] G[9] S[9] B sg13_lv_nmos w=0.15u l=0.13u ng=1 m=1 mm_ok=1
XM_9_12 D[12] G[9] S[9] B sg13_lv_nmos w=0.15u l=0.13u ng=1 m=1 mm_ok=1
XM_9_13 D[13] G[9] S[9] B sg13_lv_nmos w=0.15u l=0.13u ng=1 m=1 mm_ok=1
XM_9_14 D[14] G[9] S[9] B sg13_lv_nmos w=0.15u l=0.13u ng=1 m=1 mm_ok=1
XM_9_15 D[15] G[9] S[9] B sg13_lv_nmos w=0.15u l=0.13u ng=1 m=1 mm_ok=1
XM_9_16 D[16] G[9] S[9] B sg13_lv_nmos w=0.15u l=0.13u ng=1 m=1 mm_ok=1
XM_9_17 D[17] G[9] S[9] B sg13_lv_nmos w=0.15u l=0.13u ng=1 m=1 mm_ok=1
XM_10_0 D[0] G[10] S[10] B sg13_lv_nmos w=0.15u l=0.13u ng=1 m=1 mm_ok=1
XM_10_1 D[1] G[10] S[10] B sg13_lv_nmos w=0.15u l=0.13u ng=1 m=1 mm_ok=1
XM_10_2 D[2] G[10] S[10] B sg13_lv_nmos w=0.15u l=0.13u ng=1 m=1 mm_ok=1
XM_10_3 D[3] G[10] S[10] B sg13_lv_nmos w=0.15u l=0.13u ng=1 m=1 mm_ok=1
XM_10_4 D[4] G[10] S[10] B sg13_lv_nmos w=0.15u l=0.13u ng=1 m=1 mm_ok=1
XM_10_5 D[5] G[10] S[10] B sg13_lv_nmos w=0.15u l=0.13u ng=1 m=1 mm_ok=1
XM_10_6 D[6] G[10] S[10] B sg13_lv_nmos w=0.15u l=0.13u ng=1 m=1 mm_ok=1
XM_10_7 D[7] G[10] S[10] B sg13_lv_nmos w=0.15u l=0.13u ng=1 m=1 mm_ok=1
XM_10_8 D[8] G[10] S[10] B sg13_lv_nmos w=0.15u l=0.13u ng=1 m=1 mm_ok=1
XM_10_9 D[9] G[10] S[10] B sg13_lv_nmos w=0.15u l=0.13u ng=1 m=1 mm_ok=1
XM_10_10 D[10] G[10] S[10] B sg13_lv_nmos w=0.15u l=0.13u ng=1 m=1 mm_ok=1
XM_10_11 D[11] G[10] S[10] B sg13_lv_nmos w=0.15u l=0.13u ng=1 m=1 mm_ok=1
XM_10_12 D[12] G[10] S[10] B sg13_lv_nmos w=0.15u l=0.13u ng=1 m=1 mm_ok=1
XM_10_13 D[13] G[10] S[10] B sg13_lv_nmos w=0.15u l=0.13u ng=1 m=1 mm_ok=1
XM_10_14 D[14] G[10] S[10] B sg13_lv_nmos w=0.15u l=0.13u ng=1 m=1 mm_ok=1
XM_10_15 D[15] G[10] S[10] B sg13_lv_nmos w=0.15u l=0.13u ng=1 m=1 mm_ok=1
XM_10_16 D[16] G[10] S[10] B sg13_lv_nmos w=0.15u l=0.13u ng=1 m=1 mm_ok=1
XM_10_17 D[17] G[10] S[10] B sg13_lv_nmos w=0.15u l=0.13u ng=1 m=1 mm_ok=1
XM_11_0 D[0] G[11] S[11] B sg13_lv_nmos w=0.15u l=0.13u ng=1 m=1 mm_ok=1
XM_11_1 D[1] G[11] S[11] B sg13_lv_nmos w=0.15u l=0.13u ng=1 m=1 mm_ok=1
XM_11_2 D[2] G[11] S[11] B sg13_lv_nmos w=0.15u l=0.13u ng=1 m=1 mm_ok=1
XM_11_3 D[3] G[11] S[11] B sg13_lv_nmos w=0.15u l=0.13u ng=1 m=1 mm_ok=1
XM_11_4 D[4] G[11] S[11] B sg13_lv_nmos w=0.15u l=0.13u ng=1 m=1 mm_ok=1
XM_11_5 D[5] G[11] S[11] B sg13_lv_nmos w=0.15u l=0.13u ng=1 m=1 mm_ok=1
XM_11_6 D[6] G[11] S[11] B sg13_lv_nmos w=0.15u l=0.13u ng=1 m=1 mm_ok=1
XM_11_7 D[7] G[11] S[11] B sg13_lv_nmos w=0.15u l=0.13u ng=1 m=1 mm_ok=1
XM_11_8 D[8] G[11] S[11] B sg13_lv_nmos w=0.15u l=0.13u ng=1 m=1 mm_ok=1
XM_11_9 D[9] G[11] S[11] B sg13_lv_nmos w=0.15u l=0.13u ng=1 m=1 mm_ok=1
XM_11_10 D[10] G[11] S[11] B sg13_lv_nmos w=0.15u l=0.13u ng=1 m=1 mm_ok=1
XM_11_11 D[11] G[11] S[11] B sg13_lv_nmos w=0.15u l=0.13u ng=1 m=1 mm_ok=1
XM_11_12 D[12] G[11] S[11] B sg13_lv_nmos w=0.15u l=0.13u ng=1 m=1 mm_ok=1
XM_11_13 D[13] G[11] S[11] B sg13_lv_nmos w=0.15u l=0.13u ng=1 m=1 mm_ok=1
XM_11_14 D[14] G[11] S[11] B sg13_lv_nmos w=0.15u l=0.13u ng=1 m=1 mm_ok=1
XM_11_15 D[15] G[11] S[11] B sg13_lv_nmos w=0.15u l=0.13u ng=1 m=1 mm_ok=1
XM_11_16 D[16] G[11] S[11] B sg13_lv_nmos w=0.15u l=0.13u ng=1 m=1 mm_ok=1
XM_11_17 D[17] G[11] S[11] B sg13_lv_nmos w=0.15u l=0.13u ng=1 m=1 mm_ok=1
XM_12_0 D[0] G[12] S[12] B sg13_lv_nmos w=0.15u l=0.13u ng=1 m=1 mm_ok=1
XM_12_1 D[1] G[12] S[12] B sg13_lv_nmos w=0.15u l=0.13u ng=1 m=1 mm_ok=1
XM_12_2 D[2] G[12] S[12] B sg13_lv_nmos w=0.15u l=0.13u ng=1 m=1 mm_ok=1
XM_12_3 D[3] G[12] S[12] B sg13_lv_nmos w=0.15u l=0.13u ng=1 m=1 mm_ok=1
XM_12_4 D[4] G[12] S[12] B sg13_lv_nmos w=0.15u l=0.13u ng=1 m=1 mm_ok=1
XM_12_5 D[5] G[12] S[12] B sg13_lv_nmos w=0.15u l=0.13u ng=1 m=1 mm_ok=1
XM_12_6 D[6] G[12] S[12] B sg13_lv_nmos w=0.15u l=0.13u ng=1 m=1 mm_ok=1
XM_12_7 D[7] G[12] S[12] B sg13_lv_nmos w=0.15u l=0.13u ng=1 m=1 mm_ok=1
XM_12_8 D[8] G[12] S[12] B sg13_lv_nmos w=0.15u l=0.13u ng=1 m=1 mm_ok=1
XM_12_9 D[9] G[12] S[12] B sg13_lv_nmos w=0.15u l=0.13u ng=1 m=1 mm_ok=1
XM_12_10 D[10] G[12] S[12] B sg13_lv_nmos w=0.15u l=0.13u ng=1 m=1 mm_ok=1
XM_12_11 D[11] G[12] S[12] B sg13_lv_nmos w=0.15u l=0.13u ng=1 m=1 mm_ok=1
XM_12_12 D[12] G[12] S[12] B sg13_lv_nmos w=0.15u l=0.13u ng=1 m=1 mm_ok=1
XM_12_13 D[13] G[12] S[12] B sg13_lv_nmos w=0.15u l=0.13u ng=1 m=1 mm_ok=1
XM_12_14 D[14] G[12] S[12] B sg13_lv_nmos w=0.15u l=0.13u ng=1 m=1 mm_ok=1
XM_12_15 D[15] G[12] S[12] B sg13_lv_nmos w=0.15u l=0.13u ng=1 m=1 mm_ok=1
XM_12_16 D[16] G[12] S[12] B sg13_lv_nmos w=0.15u l=0.13u ng=1 m=1 mm_ok=1
XM_12_17 D[17] G[12] S[12] B sg13_lv_nmos w=0.15u l=0.13u ng=1 m=1 mm_ok=1
XM_13_0 D[0] G[13] S[13] B sg13_lv_nmos w=0.15u l=0.13u ng=1 m=1 mm_ok=1
XM_13_1 D[1] G[13] S[13] B sg13_lv_nmos w=0.15u l=0.13u ng=1 m=1 mm_ok=1
XM_13_2 D[2] G[13] S[13] B sg13_lv_nmos w=0.15u l=0.13u ng=1 m=1 mm_ok=1
XM_13_3 D[3] G[13] S[13] B sg13_lv_nmos w=0.15u l=0.13u ng=1 m=1 mm_ok=1
XM_13_4 D[4] G[13] S[13] B sg13_lv_nmos w=0.15u l=0.13u ng=1 m=1 mm_ok=1
XM_13_5 D[5] G[13] S[13] B sg13_lv_nmos w=0.15u l=0.13u ng=1 m=1 mm_ok=1
XM_13_6 D[6] G[13] S[13] B sg13_lv_nmos w=0.15u l=0.13u ng=1 m=1 mm_ok=1
XM_13_7 D[7] G[13] S[13] B sg13_lv_nmos w=0.15u l=0.13u ng=1 m=1 mm_ok=1
XM_13_8 D[8] G[13] S[13] B sg13_lv_nmos w=0.15u l=0.13u ng=1 m=1 mm_ok=1
XM_13_9 D[9] G[13] S[13] B sg13_lv_nmos w=0.15u l=0.13u ng=1 m=1 mm_ok=1
XM_13_10 D[10] G[13] S[13] B sg13_lv_nmos w=0.15u l=0.13u ng=1 m=1 mm_ok=1
XM_13_11 D[11] G[13] S[13] B sg13_lv_nmos w=0.15u l=0.13u ng=1 m=1 mm_ok=1
XM_13_12 D[12] G[13] S[13] B sg13_lv_nmos w=0.15u l=0.13u ng=1 m=1 mm_ok=1
XM_13_13 D[13] G[13] S[13] B sg13_lv_nmos w=0.15u l=0.13u ng=1 m=1 mm_ok=1
XM_13_14 D[14] G[13] S[13] B sg13_lv_nmos w=0.15u l=0.13u ng=1 m=1 mm_ok=1
XM_13_15 D[15] G[13] S[13] B sg13_lv_nmos w=0.15u l=0.13u ng=1 m=1 mm_ok=1
XM_13_16 D[16] G[13] S[13] B sg13_lv_nmos w=0.15u l=0.13u ng=1 m=1 mm_ok=1
XM_13_17 D[17] G[13] S[13] B sg13_lv_nmos w=0.15u l=0.13u ng=1 m=1 mm_ok=1
XM_14_0 D[0] G[14] S[14] B sg13_lv_nmos w=0.15u l=0.13u ng=1 m=1 mm_ok=1
XM_14_1 D[1] G[14] S[14] B sg13_lv_nmos w=0.15u l=0.13u ng=1 m=1 mm_ok=1
XM_14_2 D[2] G[14] S[14] B sg13_lv_nmos w=0.15u l=0.13u ng=1 m=1 mm_ok=1
XM_14_3 D[3] G[14] S[14] B sg13_lv_nmos w=0.15u l=0.13u ng=1 m=1 mm_ok=1
XM_14_4 D[4] G[14] S[14] B sg13_lv_nmos w=0.15u l=0.13u ng=1 m=1 mm_ok=1
XM_14_5 D[5] G[14] S[14] B sg13_lv_nmos w=0.15u l=0.13u ng=1 m=1 mm_ok=1
XM_14_6 D[6] G[14] S[14] B sg13_lv_nmos w=0.15u l=0.13u ng=1 m=1 mm_ok=1
XM_14_7 D[7] G[14] S[14] B sg13_lv_nmos w=0.15u l=0.13u ng=1 m=1 mm_ok=1
XM_14_8 D[8] G[14] S[14] B sg13_lv_nmos w=0.15u l=0.13u ng=1 m=1 mm_ok=1
XM_14_9 D[9] G[14] S[14] B sg13_lv_nmos w=0.15u l=0.13u ng=1 m=1 mm_ok=1
XM_14_10 D[10] G[14] S[14] B sg13_lv_nmos w=0.15u l=0.13u ng=1 m=1 mm_ok=1
XM_14_11 D[11] G[14] S[14] B sg13_lv_nmos w=0.15u l=0.13u ng=1 m=1 mm_ok=1
XM_14_12 D[12] G[14] S[14] B sg13_lv_nmos w=0.15u l=0.13u ng=1 m=1 mm_ok=1
XM_14_13 D[13] G[14] S[14] B sg13_lv_nmos w=0.15u l=0.13u ng=1 m=1 mm_ok=1
XM_14_14 D[14] G[14] S[14] B sg13_lv_nmos w=0.15u l=0.13u ng=1 m=1 mm_ok=1
XM_14_15 D[15] G[14] S[14] B sg13_lv_nmos w=0.15u l=0.13u ng=1 m=1 mm_ok=1
XM_14_16 D[16] G[14] S[14] B sg13_lv_nmos w=0.15u l=0.13u ng=1 m=1 mm_ok=1
XM_14_17 D[17] G[14] S[14] B sg13_lv_nmos w=0.15u l=0.13u ng=1 m=1 mm_ok=1
XM_15_0 D[0] G[15] S[15] B sg13_lv_nmos w=0.15u l=0.13u ng=1 m=1 mm_ok=1
XM_15_1 D[1] G[15] S[15] B sg13_lv_nmos w=0.15u l=0.13u ng=1 m=1 mm_ok=1
XM_15_2 D[2] G[15] S[15] B sg13_lv_nmos w=0.15u l=0.13u ng=1 m=1 mm_ok=1
XM_15_3 D[3] G[15] S[15] B sg13_lv_nmos w=0.15u l=0.13u ng=1 m=1 mm_ok=1
XM_15_4 D[4] G[15] S[15] B sg13_lv_nmos w=0.15u l=0.13u ng=1 m=1 mm_ok=1
XM_15_5 D[5] G[15] S[15] B sg13_lv_nmos w=0.15u l=0.13u ng=1 m=1 mm_ok=1
XM_15_6 D[6] G[15] S[15] B sg13_lv_nmos w=0.15u l=0.13u ng=1 m=1 mm_ok=1
XM_15_7 D[7] G[15] S[15] B sg13_lv_nmos w=0.15u l=0.13u ng=1 m=1 mm_ok=1
XM_15_8 D[8] G[15] S[15] B sg13_lv_nmos w=0.15u l=0.13u ng=1 m=1 mm_ok=1
XM_15_9 D[9] G[15] S[15] B sg13_lv_nmos w=0.15u l=0.13u ng=1 m=1 mm_ok=1
XM_15_10 D[10] G[15] S[15] B sg13_lv_nmos w=0.15u l=0.13u ng=1 m=1 mm_ok=1
XM_15_11 D[11] G[15] S[15] B sg13_lv_nmos w=0.15u l=0.13u ng=1 m=1 mm_ok=1
XM_15_12 D[12] G[15] S[15] B sg13_lv_nmos w=0.15u l=0.13u ng=1 m=1 mm_ok=1
XM_15_13 D[13] G[15] S[15] B sg13_lv_nmos w=0.15u l=0.13u ng=1 m=1 mm_ok=1
XM_15_14 D[14] G[15] S[15] B sg13_lv_nmos w=0.15u l=0.13u ng=1 m=1 mm_ok=1
XM_15_15 D[15] G[15] S[15] B sg13_lv_nmos w=0.15u l=0.13u ng=1 m=1 mm_ok=1
XM_15_16 D[16] G[15] S[15] B sg13_lv_nmos w=0.15u l=0.13u ng=1 m=1 mm_ok=1
XM_15_17 D[17] G[15] S[15] B sg13_lv_nmos w=0.15u l=0.13u ng=1 m=1 mm_ok=1
XM_16_0 D[0] G[16] S[16] B sg13_lv_nmos w=0.15u l=0.13u ng=1 m=1 mm_ok=1
XM_16_1 D[1] G[16] S[16] B sg13_lv_nmos w=0.15u l=0.13u ng=1 m=1 mm_ok=1
XM_16_2 D[2] G[16] S[16] B sg13_lv_nmos w=0.15u l=0.13u ng=1 m=1 mm_ok=1
XM_16_3 D[3] G[16] S[16] B sg13_lv_nmos w=0.15u l=0.13u ng=1 m=1 mm_ok=1
XM_16_4 D[4] G[16] S[16] B sg13_lv_nmos w=0.15u l=0.13u ng=1 m=1 mm_ok=1
XM_16_5 D[5] G[16] S[16] B sg13_lv_nmos w=0.15u l=0.13u ng=1 m=1 mm_ok=1
XM_16_6 D[6] G[16] S[16] B sg13_lv_nmos w=0.15u l=0.13u ng=1 m=1 mm_ok=1
XM_16_7 D[7] G[16] S[16] B sg13_lv_nmos w=0.15u l=0.13u ng=1 m=1 mm_ok=1
XM_16_8 D[8] G[16] S[16] B sg13_lv_nmos w=0.15u l=0.13u ng=1 m=1 mm_ok=1
XM_16_9 D[9] G[16] S[16] B sg13_lv_nmos w=0.15u l=0.13u ng=1 m=1 mm_ok=1
XM_16_10 D[10] G[16] S[16] B sg13_lv_nmos w=0.15u l=0.13u ng=1 m=1 mm_ok=1
XM_16_11 D[11] G[16] S[16] B sg13_lv_nmos w=0.15u l=0.13u ng=1 m=1 mm_ok=1
XM_16_12 D[12] G[16] S[16] B sg13_lv_nmos w=0.15u l=0.13u ng=1 m=1 mm_ok=1
XM_16_13 D[13] G[16] S[16] B sg13_lv_nmos w=0.15u l=0.13u ng=1 m=1 mm_ok=1
XM_16_14 D[14] G[16] S[16] B sg13_lv_nmos w=0.15u l=0.13u ng=1 m=1 mm_ok=1
XM_16_15 D[15] G[16] S[16] B sg13_lv_nmos w=0.15u l=0.13u ng=1 m=1 mm_ok=1
XM_16_16 D[16] G[16] S[16] B sg13_lv_nmos w=0.15u l=0.13u ng=1 m=1 mm_ok=1
XM_16_17 D[17] G[16] S[16] B sg13_lv_nmos w=0.15u l=0.13u ng=1 m=1 mm_ok=1
XM_17_0 D[0] G[17] S[17] B sg13_lv_nmos w=0.15u l=0.13u ng=1 m=1 mm_ok=1
XM_17_1 D[1] G[17] S[17] B sg13_lv_nmos w=0.15u l=0.13u ng=1 m=1 mm_ok=1
XM_17_2 D[2] G[17] S[17] B sg13_lv_nmos w=0.15u l=0.13u ng=1 m=1 mm_ok=1
XM_17_3 D[3] G[17] S[17] B sg13_lv_nmos w=0.15u l=0.13u ng=1 m=1 mm_ok=1
XM_17_4 D[4] G[17] S[17] B sg13_lv_nmos w=0.15u l=0.13u ng=1 m=1 mm_ok=1
XM_17_5 D[5] G[17] S[17] B sg13_lv_nmos w=0.15u l=0.13u ng=1 m=1 mm_ok=1
XM_17_6 D[6] G[17] S[17] B sg13_lv_nmos w=0.15u l=0.13u ng=1 m=1 mm_ok=1
XM_17_7 D[7] G[17] S[17] B sg13_lv_nmos w=0.15u l=0.13u ng=1 m=1 mm_ok=1
XM_17_8 D[8] G[17] S[17] B sg13_lv_nmos w=0.15u l=0.13u ng=1 m=1 mm_ok=1
XM_17_9 D[9] G[17] S[17] B sg13_lv_nmos w=0.15u l=0.13u ng=1 m=1 mm_ok=1
XM_17_10 D[10] G[17] S[17] B sg13_lv_nmos w=0.15u l=0.13u ng=1 m=1 mm_ok=1
XM_17_11 D[11] G[17] S[17] B sg13_lv_nmos w=0.15u l=0.13u ng=1 m=1 mm_ok=1
XM_17_12 D[12] G[17] S[17] B sg13_lv_nmos w=0.15u l=0.13u ng=1 m=1 mm_ok=1
XM_17_13 D[13] G[17] S[17] B sg13_lv_nmos w=0.15u l=0.13u ng=1 m=1 mm_ok=1
XM_17_14 D[14] G[17] S[17] B sg13_lv_nmos w=0.15u l=0.13u ng=1 m=1 mm_ok=1
XM_17_15 D[15] G[17] S[17] B sg13_lv_nmos w=0.15u l=0.13u ng=1 m=1 mm_ok=1
XM_17_16 D[16] G[17] S[17] B sg13_lv_nmos w=0.15u l=0.13u ng=1 m=1 mm_ok=1
XM_17_17 D[17] G[17] S[17] B sg13_lv_nmos w=0.15u l=0.13u ng=1 m=1 mm_ok=1
**.ends
.end
